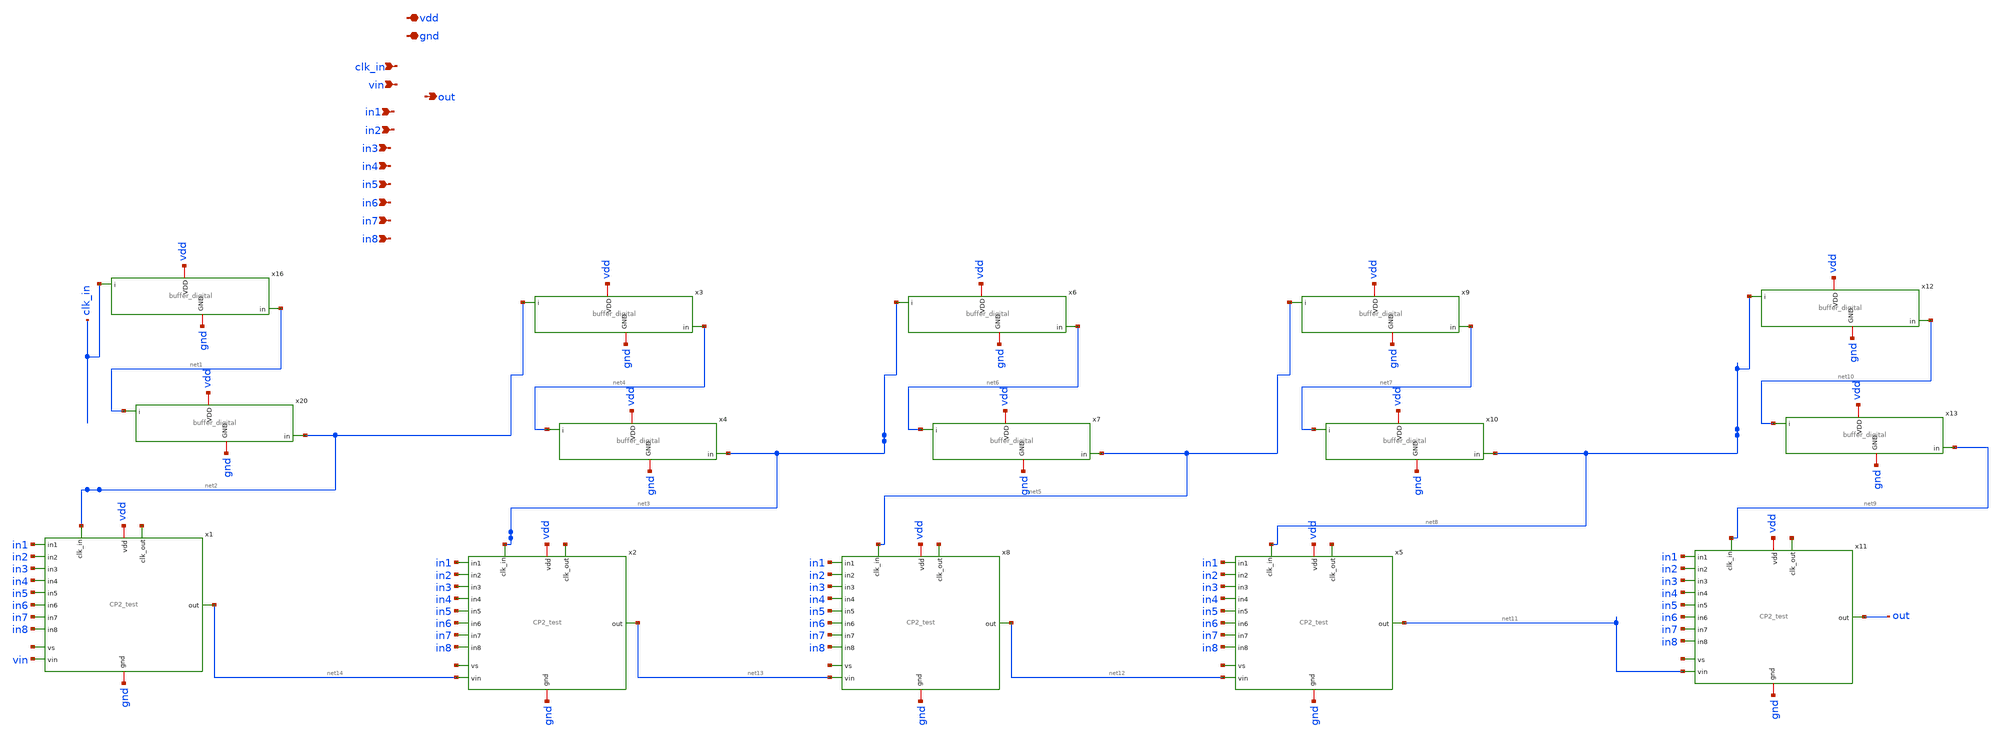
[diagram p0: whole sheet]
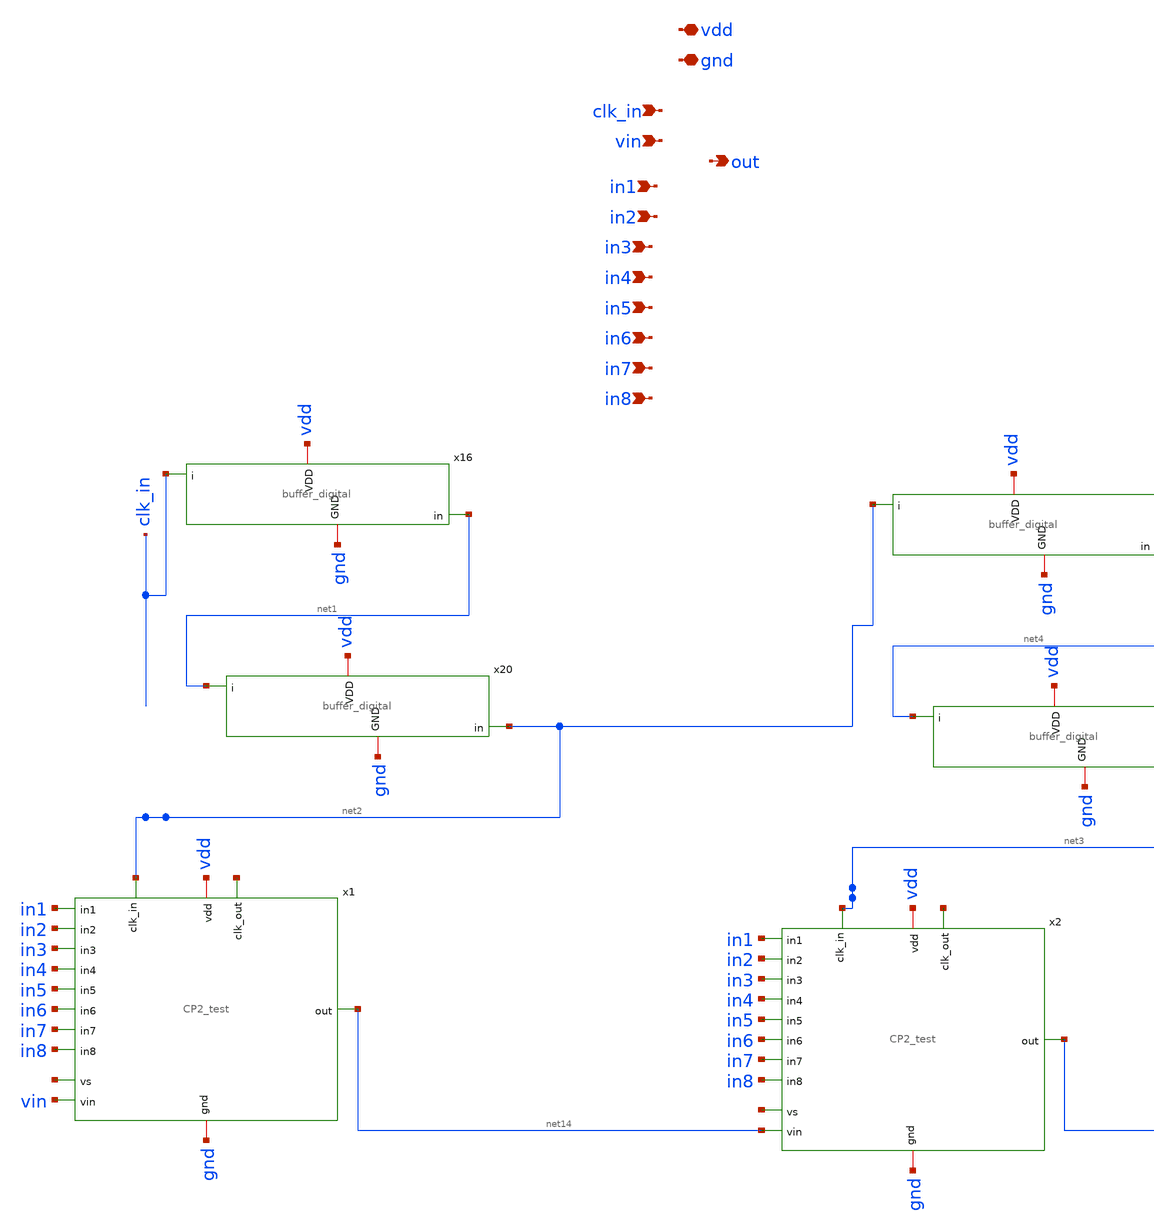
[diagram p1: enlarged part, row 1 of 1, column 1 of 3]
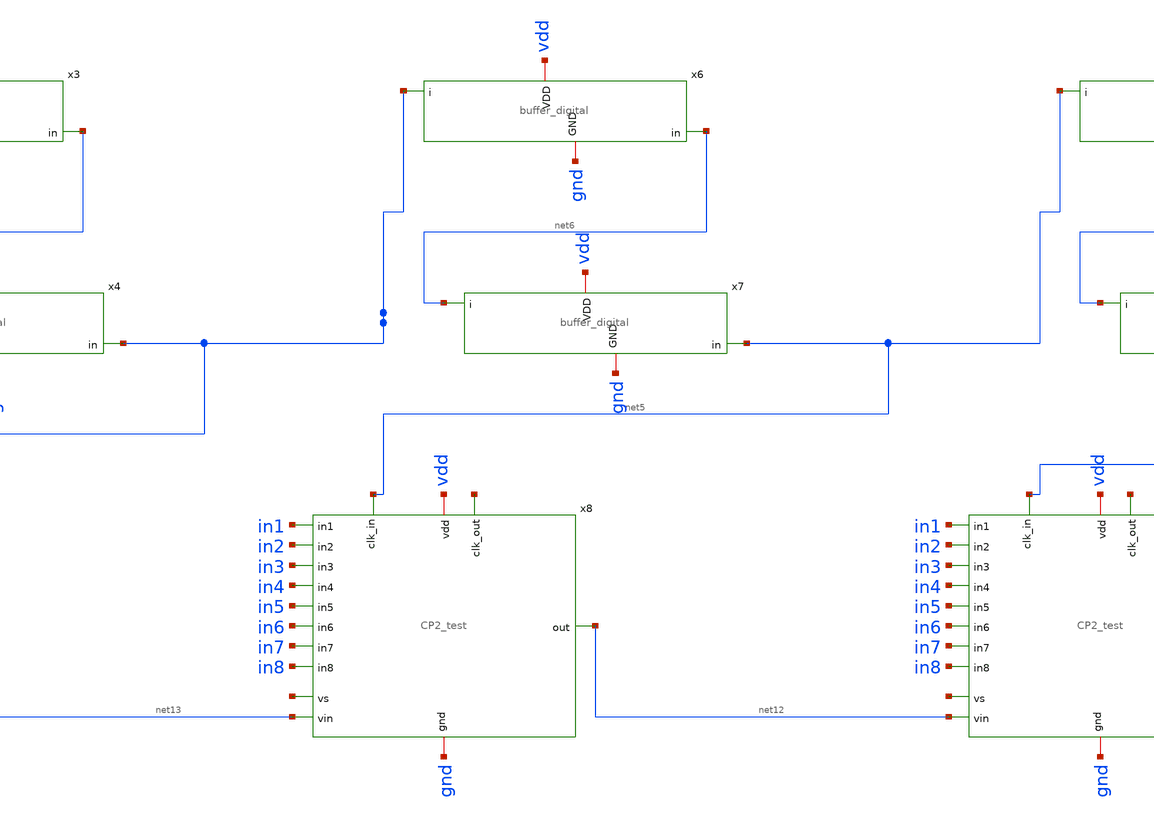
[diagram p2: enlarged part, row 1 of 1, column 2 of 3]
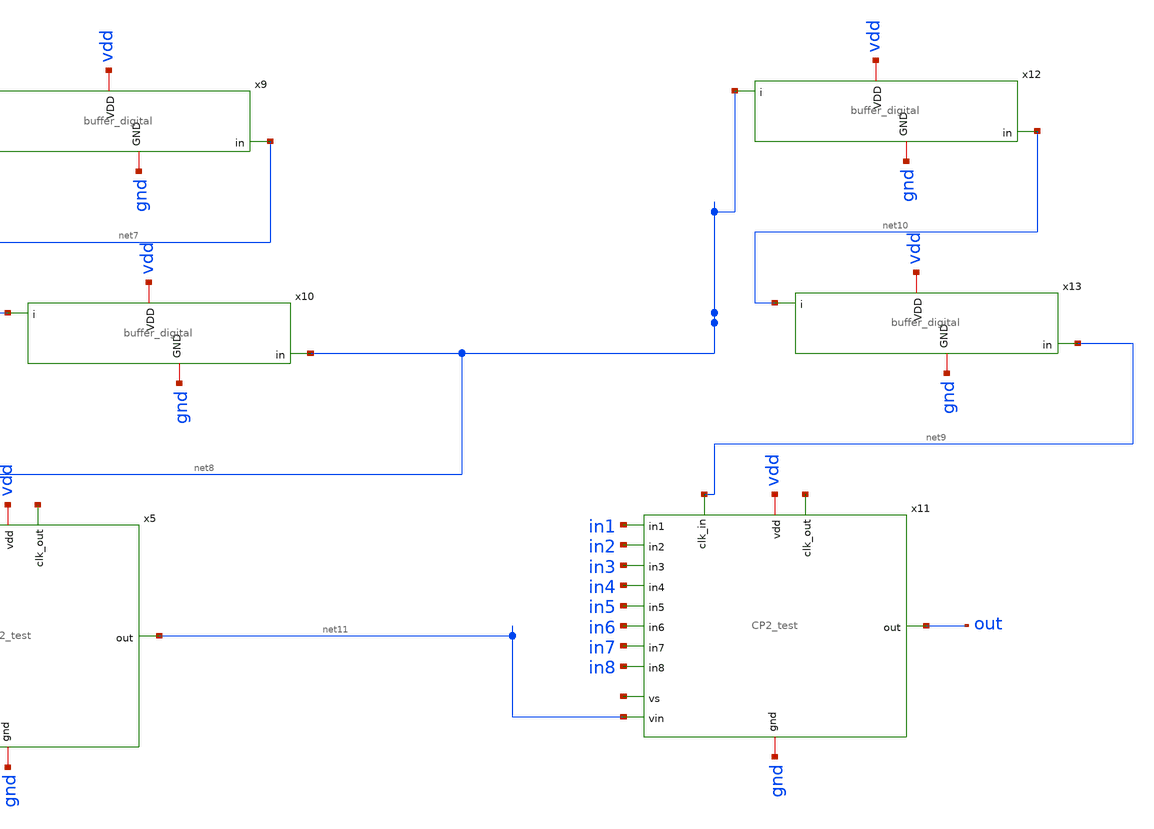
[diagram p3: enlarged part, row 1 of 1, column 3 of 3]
** sch_path: xschem/charge_pumps2/cp2_buffer_5stage_xschem.sch
**.subckt cp2_buffer_5stage_xschem clk_in gnd vdd out vin in1 in2 in3 in4 in5 in6 in7 in8
*.ipin clk_in
*.iopin gnd
*.iopin vdd
*.opin out
*.ipin vin
*.ipin in1
*.ipin in2
*.ipin in3
*.ipin in4
*.ipin in5
*.ipin in6
*.ipin in7
*.ipin in8
x16 gnd vdd clk_in net1 buffer_digital
x20 gnd vdd net1 net2 buffer_digital
x3 gnd vdd net2 net4 buffer_digital
x4 gnd vdd net4 net3 buffer_digital
x6 gnd vdd net3 net6 buffer_digital
x7 gnd vdd net6 net5 buffer_digital
x9 gnd vdd net5 net7 buffer_digital
x10 gnd vdd net7 net8 buffer_digital
x12 gnd vdd net8 net10 buffer_digital
x13 gnd vdd net10 net9 buffer_digital
x1 gnd net15 net2 vin net14 in1 in2 in3 in4 in5 in6 in7 in8 vdd net16 CP2_test
x2 gnd net17 net3 net14 net13 in1 in2 in3 in4 in5 in6 in7 in8 vdd net18 CP2_test
x5 gnd net19 net8 net12 net11 in1 in2 in3 in4 in5 in6 in7 in8 vdd net20 CP2_test
x8 gnd net21 net5 net13 net12 in1 in2 in3 in4 in5 in6 in7 in8 vdd net22 CP2_test
x11 gnd net23 net9 net11 out in1 in2 in3 in4 in5 in6 in7 in8 vdd net24 CP2_test
**.ends
.end
